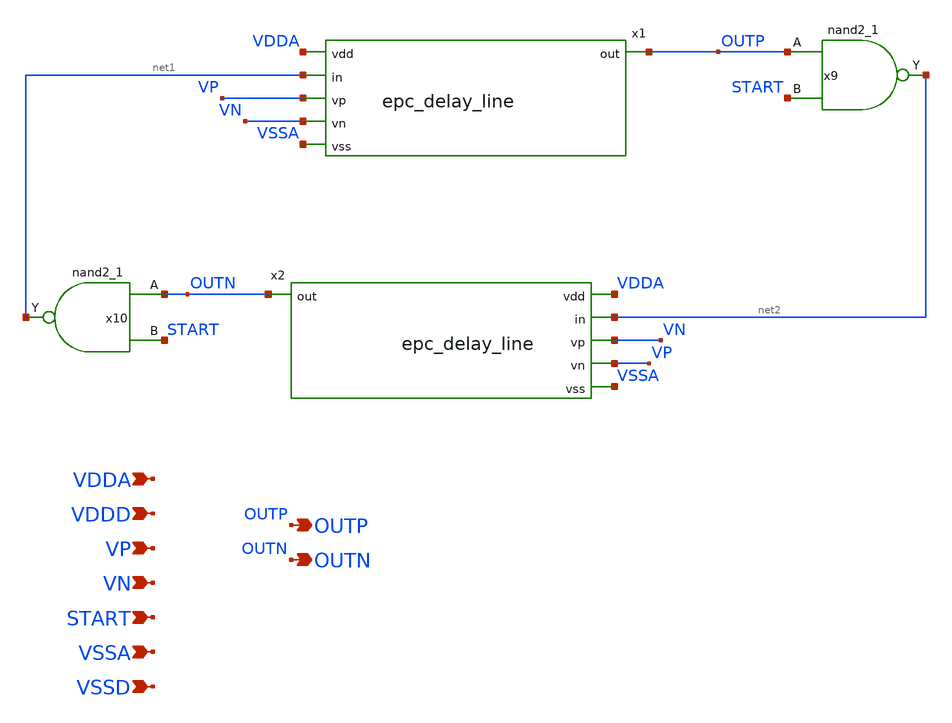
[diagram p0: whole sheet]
** sch_path: xschem/epc.sch
**.subckt epc VDDD VP VN VSSA OUTP START OUTN VDDA VSSD
*.ipin VDDD
*.ipin VP
*.ipin VN
*.ipin VSSA
*.opin OUTP
*.ipin START
*.opin OUTN
*.ipin VDDA
*.ipin VSSD
x9 OUTP START VSSD VSSD VDDD VDDD net2 sky130_fd_sc_hd__nand2_1
x10 OUTN START VSSD VSSD VDDD VDDD net1 sky130_fd_sc_hd__nand2_1
x1 VDDA net1 VP VN VSSA OUTP epc_delay_line
x2 VDDA net2 VN VP VSSA OUTN epc_delay_line
**.ends

* expanding   symbol:  epc_delay_line.sym # of pins=6
** sym_path: epc_delay_line.sym
** sch_path: epc_delay_line.sch
.subckt epc_delay_line vdd in vp vn vss out
*.ipin vdd
*.ipin in
*.ipin vp
*.ipin vn
*.ipin vss
*.opin out
x1 in net1 vp vdd vss epc_delay
x2 net1 net2 vn vdd vss epc_delay
x3 net2 net3 vp vdd vss epc_delay
x4 net3 net4 vn vdd vss epc_delay
x5 net4 net5 vp vdd vss epc_delay
x6 net5 net6 vn vdd vss epc_delay
x7 net6 net7 vp vdd vss epc_delay
x8 net7 out vn vdd vss epc_delay
.ends


* expanding   symbol:  epc_delay.sym # of pins=5
** sym_path: epc_delay.sym
** sch_path: epc_delay.sch
.subckt epc_delay IN OUT VIN VDD VSS
*.ipin VDD
*.ipin VIN
*.ipin IN
*.ipin VSS
*.opin OUT
.param W_P=9 W_N=3 L_N=0.4 L_P=0.4
XM1 net2 VIN VDD VDD sky130_fd_pr__pfet_01v8_lvt L=L_P W=W_P nf=1 ad='int((nf+1)/2) * W/nf * 0.29' as='int((nf+2)/2) * W/nf * 0.29'
+ pd='2*int((nf+1)/2) * (W/nf + 0.29)' ps='2*int((nf+2)/2) * (W/nf + 0.29)' nrd='0.29 / W' nrs='0.29 / W'
+ sa=0 sb=0 sd=0 mult=1 m=1
XM2 OUT IN net2 VDD sky130_fd_pr__pfet_01v8_lvt L=L_P W=W_P nf=1 ad='int((nf+1)/2) * W/nf * 0.29' as='int((nf+2)/2) * W/nf * 0.29'
+ pd='2*int((nf+1)/2) * (W/nf + 0.29)' ps='2*int((nf+2)/2) * (W/nf + 0.29)' nrd='0.29 / W' nrs='0.29 / W'
+ sa=0 sb=0 sd=0 mult=1 m=1
XM3 OUT IN net1 VSS sky130_fd_pr__nfet_01v8_lvt L=L_N W=W_N nf=1 ad='int((nf+1)/2) * W/nf * 0.29' as='int((nf+2)/2) * W/nf * 0.29'
+ pd='2*int((nf+1)/2) * (W/nf + 0.29)' ps='2*int((nf+2)/2) * (W/nf + 0.29)' nrd='0.29 / W' nrs='0.29 / W'
+ sa=0 sb=0 sd=0 mult=1 m=1
XM4 net1 VIN VSS VSS sky130_fd_pr__nfet_01v8_lvt L=L_N W=W_N nf=1 ad='int((nf+1)/2) * W/nf * 0.29' as='int((nf+2)/2) * W/nf * 0.29'
+ pd='2*int((nf+1)/2) * (W/nf + 0.29)' ps='2*int((nf+2)/2) * (W/nf + 0.29)' nrd='0.29 / W' nrs='0.29 / W'
+ sa=0 sb=0 sd=0 mult=1 m=1
.ends

.end
